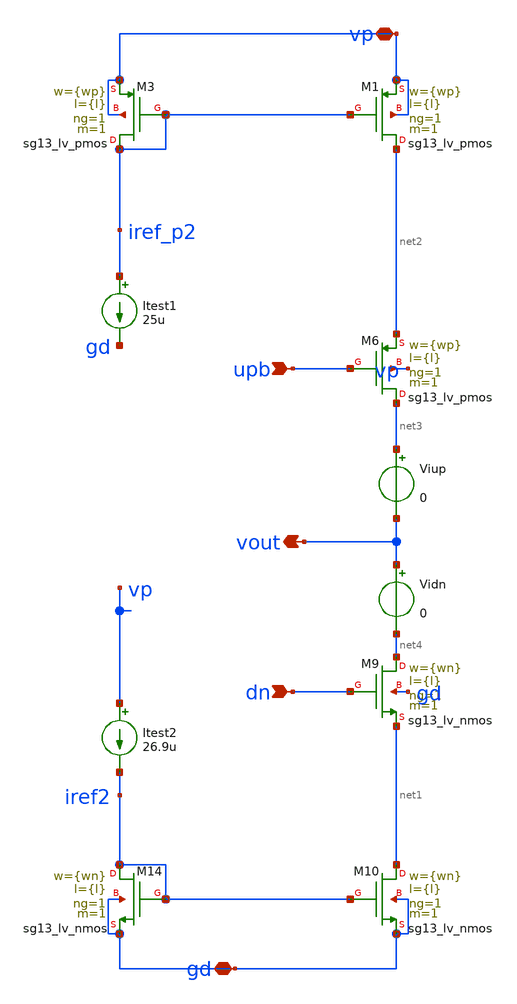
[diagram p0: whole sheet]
** sch_path: charge_pump/cp2_simple_ideal.sch
**.subckt cp2_simple_ideal vp upb vout dn gd
*.iopin vp
*.ipin upb
*.opin vout
*.ipin dn
*.iopin gd
XM3 iref_p2 iref_p2 vp vp sg13_lv_pmos w={wp} l={l} ng=1 m=1 mm_ok=1
XM1 net2 iref_p2 vp vp sg13_lv_pmos w={wp} l={l} ng=1 m=1 mm_ok=1
XM6 net3 upb net2 vp sg13_lv_pmos w={wp} l={l} ng=1 m=1 mm_ok=1
XM9 net4 dn net1 gd sg13_lv_nmos w={wn} l={l} ng=1 m=1 mm_ok=1
XM10 net1 iref2 gd gd sg13_lv_nmos w={wn} l={l} ng=1 m=1 mm_ok=1
XM14 iref2 iref2 gd gd sg13_lv_nmos w={wn} l={l} ng=1 m=1 mm_ok=1
Itest1 iref_p2 gd 25u
Itest2 vp iref2 26.9u
Vidn vout net4 0
Viup net3 vout 0
**.ends
.end
